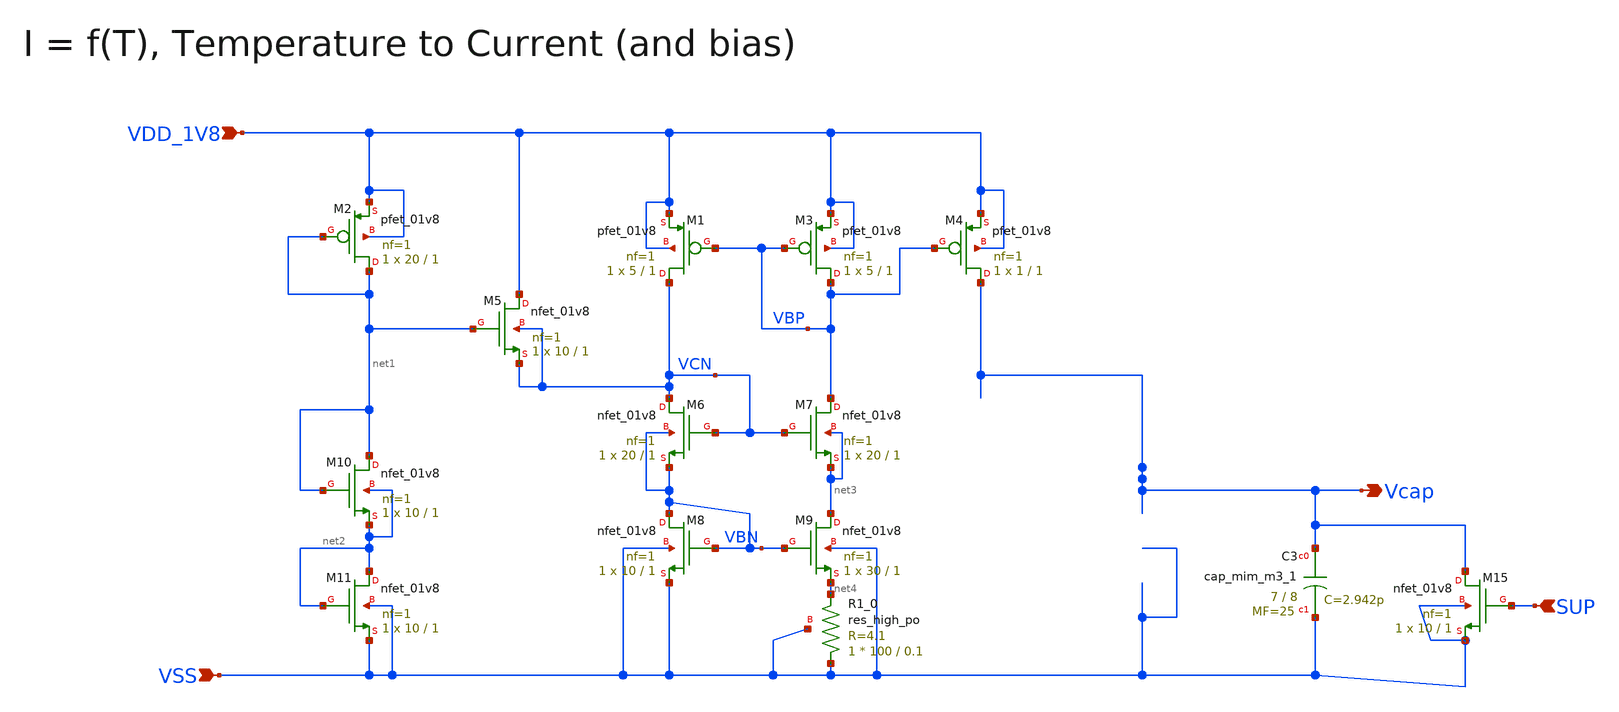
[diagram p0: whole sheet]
** sch_path: design/CNR_GR06_SKY130NM/CNR_GR06.sch
**.subckt CNR_GR06 VDD_1V8 VSS Vcap SUP
*.ipin VDD_1V8
*.ipin VSS
*.opin Vcap
*.ipin SUP
XM5 VDD_1V8 net1 VCN VCN sky130_fd_pr__nfet_01v8 L=1 W=10 nf=1 ad='int((nf+1)/2) * W/nf * 0.29' as='int((nf+2)/2) * W/nf * 0.29'
+ pd='2*int((nf+1)/2) * (W/nf + 0.29)' ps='2*int((nf+2)/2) * (W/nf + 0.29)' nrd='0.29 / W' nrs='0.29 / W'
+ sa=0 sb=0 sd=0 mult=1 m=1
XM2 net1 net1 VDD_1V8 VDD_1V8 sky130_fd_pr__pfet_01v8 L=1 W=20 nf=1 ad='int((nf+1)/2) * W/nf * 0.29'
+ as='int((nf+2)/2) * W/nf * 0.29' pd='2*int((nf+1)/2) * (W/nf + 0.29)' ps='2*int((nf+2)/2) * (W/nf + 0.29)'
+ nrd='0.29 / W' nrs='0.29 / W' sa=0 sb=0 sd=0 mult=1 m=1
XM1 VCN VBP VDD_1V8 VDD_1V8 sky130_fd_pr__pfet_01v8 L=1 W=5 nf=1 ad='int((nf+1)/2) * W/nf * 0.29' as='int((nf+2)/2) * W/nf * 0.29'
+ pd='2*int((nf+1)/2) * (W/nf + 0.29)' ps='2*int((nf+2)/2) * (W/nf + 0.29)' nrd='0.29 / W' nrs='0.29 / W'
+ sa=0 sb=0 sd=0 mult=1 m=1
XM3 VBP VBP VDD_1V8 VDD_1V8 sky130_fd_pr__pfet_01v8 L=1 W=5 nf=1 ad='int((nf+1)/2) * W/nf * 0.29' as='int((nf+2)/2) * W/nf * 0.29'
+ pd='2*int((nf+1)/2) * (W/nf + 0.29)' ps='2*int((nf+2)/2) * (W/nf + 0.29)' nrd='0.29 / W' nrs='0.29 / W'
+ sa=0 sb=0 sd=0 mult=1 m=1
XM4 Vcap VBP VDD_1V8 VDD_1V8 sky130_fd_pr__pfet_01v8 L=1 W=1 nf=1 ad='int((nf+1)/2) * W/nf * 0.29' as='int((nf+2)/2) * W/nf * 0.29'
+ pd='2*int((nf+1)/2) * (W/nf + 0.29)' ps='2*int((nf+2)/2) * (W/nf + 0.29)' nrd='0.29 / W' nrs='0.29 / W'
+ sa=0 sb=0 sd=0 mult=1 m=1
XM6 VCN VCN VBN VBN sky130_fd_pr__nfet_01v8 L=1 W=20 nf=1 ad='int((nf+1)/2) * W/nf * 0.29' as='int((nf+2)/2) * W/nf * 0.29'
+ pd='2*int((nf+1)/2) * (W/nf + 0.29)' ps='2*int((nf+2)/2) * (W/nf + 0.29)' nrd='0.29 / W' nrs='0.29 / W'
+ sa=0 sb=0 sd=0 mult=1 m=1
XM7 VBP VCN net3 net3 sky130_fd_pr__nfet_01v8 L=1 W=20 nf=1 ad='int((nf+1)/2) * W/nf * 0.29' as='int((nf+2)/2) * W/nf * 0.29'
+ pd='2*int((nf+1)/2) * (W/nf + 0.29)' ps='2*int((nf+2)/2) * (W/nf + 0.29)' nrd='0.29 / W' nrs='0.29 / W'
+ sa=0 sb=0 sd=0 mult=1 m=1
XM8 VBN VBN VSS VSS sky130_fd_pr__nfet_01v8 L=1 W=10 nf=1 ad='int((nf+1)/2) * W/nf * 0.29' as='int((nf+2)/2) * W/nf * 0.29'
+ pd='2*int((nf+1)/2) * (W/nf + 0.29)' ps='2*int((nf+2)/2) * (W/nf + 0.29)' nrd='0.29 / W' nrs='0.29 / W'
+ sa=0 sb=0 sd=0 mult=1 m=1
XM9 net3 VBN net4 VSS sky130_fd_pr__nfet_01v8 L=1 W=30 nf=1 ad='int((nf+1)/2) * W/nf * 0.29' as='int((nf+2)/2) * W/nf * 0.29'
+ pd='2*int((nf+1)/2) * (W/nf + 0.29)' ps='2*int((nf+2)/2) * (W/nf + 0.29)' nrd='0.29 / W' nrs='0.29 / W'
+ sa=0 sb=0 sd=0 mult=1 m=1
XM10 net1 net1 net2 net2 sky130_fd_pr__nfet_01v8 L=1 W=10 nf=1 ad='int((nf+1)/2) * W/nf * 0.29' as='int((nf+2)/2) * W/nf * 0.29'
+ pd='2*int((nf+1)/2) * (W/nf + 0.29)' ps='2*int((nf+2)/2) * (W/nf + 0.29)' nrd='0.29 / W' nrs='0.29 / W'
+ sa=0 sb=0 sd=0 mult=1 m=1
XM11 net2 net2 VSS VSS sky130_fd_pr__nfet_01v8 L=1 W=10 nf=1 ad='int((nf+1)/2) * W/nf * 0.29' as='int((nf+2)/2) * W/nf * 0.29'
+ pd='2*int((nf+1)/2) * (W/nf + 0.29)' ps='2*int((nf+2)/2) * (W/nf + 0.29)' nrd='0.29 / W' nrs='0.29 / W'
+ sa=0 sb=0 sd=0 mult=1 m=1
XC3 Vcap VSS sky130_fd_pr__cap_mim_m3_1 W=7 L=8 MF=25 m=25
XR1_0 VSS net4 VSS sky130_fd_pr__res_high_po W=100 L=0.1 mult=1 m=1
XM15 Vcap SUP VSS VSS sky130_fd_pr__nfet_01v8 L=1 W=10 nf=1 ad='int((nf+1)/2) * W/nf * 0.29' as='int((nf+2)/2) * W/nf * 0.29'
+ pd='2*int((nf+1)/2) * (W/nf + 0.29)' ps='2*int((nf+2)/2) * (W/nf + 0.29)' nrd='0.29 / W' nrs='0.29 / W'
+ sa=0 sb=0 sd=0 mult=1 m=1
**.ends
.end
